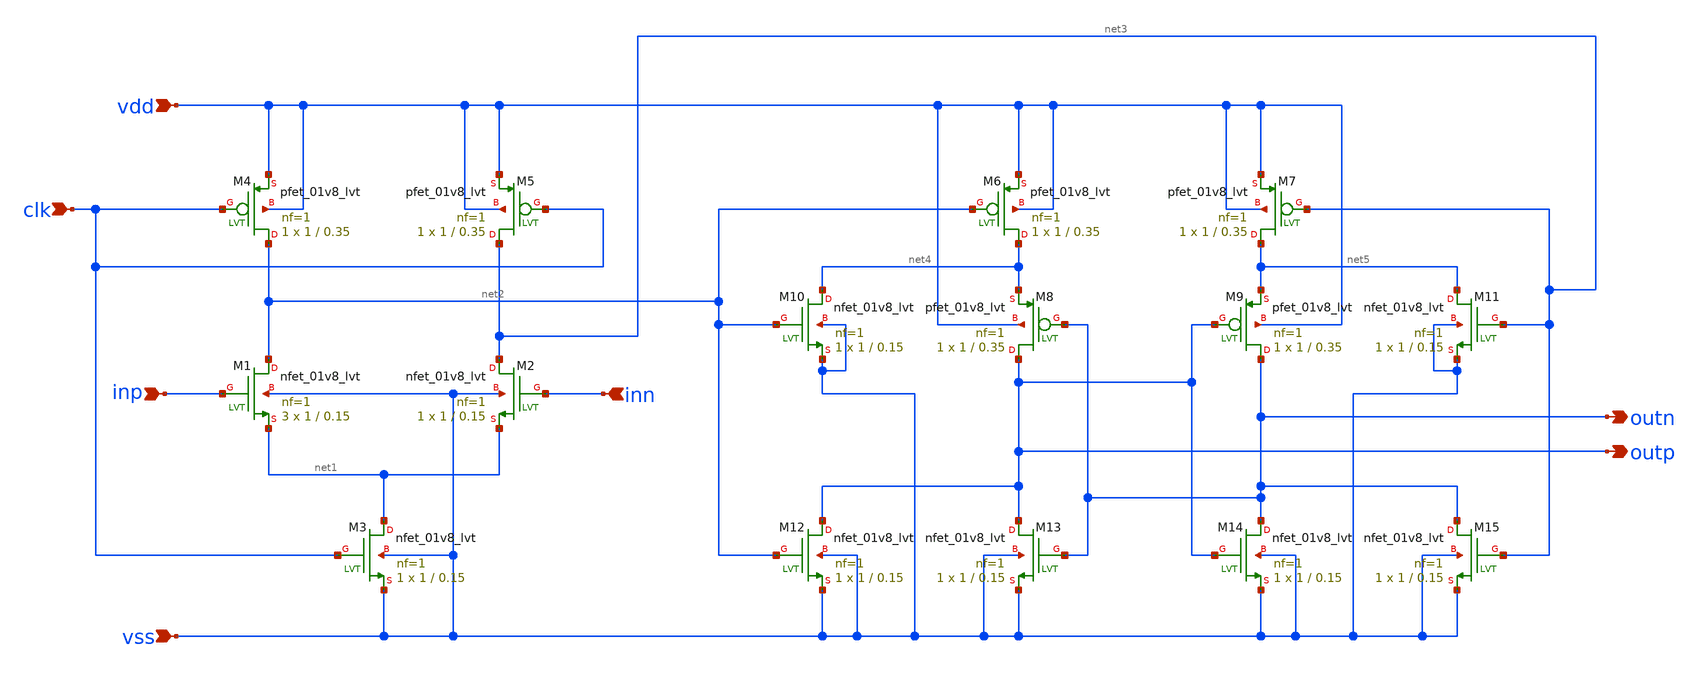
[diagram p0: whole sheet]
** sch_path: xschem/my_dynamic_comparator2.sch
**.subckt my_dynamic_comparator2 clk inn inp vdd vss outn outp
*.ipin clk
*.ipin inn
*.ipin inp
*.ipin vdd
*.ipin vss
*.opin outn
*.opin outp
XM1 net2 inp net1 vss sky130_fd_pr__nfet_01v8_lvt L=0.15 W=1 nf=1 ad='int((nf+1)/2) * W/nf * 0.29' as='int((nf+2)/2) * W/nf * 0.29'
+ pd='2*int((nf+1)/2) * (W/nf + 0.29)' ps='2*int((nf+2)/2) * (W/nf + 0.29)' nrd='0.29 / W' nrs='0.29 / W'
+ sa=0 sb=0 sd=0 mult=3 m=3
XM2 net3 inn net1 vss sky130_fd_pr__nfet_01v8_lvt L=0.15 W=1 nf=1 ad='int((nf+1)/2) * W/nf * 0.29' as='int((nf+2)/2) * W/nf * 0.29'
+ pd='2*int((nf+1)/2) * (W/nf + 0.29)' ps='2*int((nf+2)/2) * (W/nf + 0.29)' nrd='0.29 / W' nrs='0.29 / W'
+ sa=0 sb=0 sd=0 mult=1 m=1
XM3 net1 clk vss vss sky130_fd_pr__nfet_01v8_lvt L=0.15 W=1 nf=1 ad='int((nf+1)/2) * W/nf * 0.29' as='int((nf+2)/2) * W/nf * 0.29'
+ pd='2*int((nf+1)/2) * (W/nf + 0.29)' ps='2*int((nf+2)/2) * (W/nf + 0.29)' nrd='0.29 / W' nrs='0.29 / W'
+ sa=0 sb=0 sd=0 mult=1 m=1
XM4 net2 clk vdd vdd sky130_fd_pr__pfet_01v8_lvt L=0.35 W=1 nf=1 ad='int((nf+1)/2) * W/nf * 0.29' as='int((nf+2)/2) * W/nf * 0.29'
+ pd='2*int((nf+1)/2) * (W/nf + 0.29)' ps='2*int((nf+2)/2) * (W/nf + 0.29)' nrd='0.29 / W' nrs='0.29 / W'
+ sa=0 sb=0 sd=0 mult=1 m=1
XM5 net3 clk vdd vdd sky130_fd_pr__pfet_01v8_lvt L=0.35 W=1 nf=1 ad='int((nf+1)/2) * W/nf * 0.29' as='int((nf+2)/2) * W/nf * 0.29'
+ pd='2*int((nf+1)/2) * (W/nf + 0.29)' ps='2*int((nf+2)/2) * (W/nf + 0.29)' nrd='0.29 / W' nrs='0.29 / W'
+ sa=0 sb=0 sd=0 mult=1 m=1
XM6 net4 net2 vdd vdd sky130_fd_pr__pfet_01v8_lvt L=0.35 W=1 nf=1 ad='int((nf+1)/2) * W/nf * 0.29' as='int((nf+2)/2) * W/nf * 0.29'
+ pd='2*int((nf+1)/2) * (W/nf + 0.29)' ps='2*int((nf+2)/2) * (W/nf + 0.29)' nrd='0.29 / W' nrs='0.29 / W'
+ sa=0 sb=0 sd=0 mult=1 m=1
XM7 net5 net3 vdd vdd sky130_fd_pr__pfet_01v8_lvt L=0.35 W=1 nf=1 ad='int((nf+1)/2) * W/nf * 0.29' as='int((nf+2)/2) * W/nf * 0.29'
+ pd='2*int((nf+1)/2) * (W/nf + 0.29)' ps='2*int((nf+2)/2) * (W/nf + 0.29)' nrd='0.29 / W' nrs='0.29 / W'
+ sa=0 sb=0 sd=0 mult=1 m=1
XM8 outp outn net4 vdd sky130_fd_pr__pfet_01v8_lvt L=0.35 W=1 nf=1 ad='int((nf+1)/2) * W/nf * 0.29' as='int((nf+2)/2) * W/nf * 0.29'
+ pd='2*int((nf+1)/2) * (W/nf + 0.29)' ps='2*int((nf+2)/2) * (W/nf + 0.29)' nrd='0.29 / W' nrs='0.29 / W'
+ sa=0 sb=0 sd=0 mult=1 m=1
XM9 outn outp net5 vdd sky130_fd_pr__pfet_01v8_lvt L=0.35 W=1 nf=1 ad='int((nf+1)/2) * W/nf * 0.29' as='int((nf+2)/2) * W/nf * 0.29'
+ pd='2*int((nf+1)/2) * (W/nf + 0.29)' ps='2*int((nf+2)/2) * (W/nf + 0.29)' nrd='0.29 / W' nrs='0.29 / W'
+ sa=0 sb=0 sd=0 mult=1 m=1
XM10 net4 net2 vss vss sky130_fd_pr__nfet_01v8_lvt L=0.15 W=1 nf=1 ad='int((nf+1)/2) * W/nf * 0.29' as='int((nf+2)/2) * W/nf * 0.29'
+ pd='2*int((nf+1)/2) * (W/nf + 0.29)' ps='2*int((nf+2)/2) * (W/nf + 0.29)' nrd='0.29 / W' nrs='0.29 / W'
+ sa=0 sb=0 sd=0 mult=1 m=1
XM11 net5 net3 vss vss sky130_fd_pr__nfet_01v8_lvt L=0.15 W=1 nf=1 ad='int((nf+1)/2) * W/nf * 0.29' as='int((nf+2)/2) * W/nf * 0.29'
+ pd='2*int((nf+1)/2) * (W/nf + 0.29)' ps='2*int((nf+2)/2) * (W/nf + 0.29)' nrd='0.29 / W' nrs='0.29 / W'
+ sa=0 sb=0 sd=0 mult=1 m=1
XM12 outp net2 vss vss sky130_fd_pr__nfet_01v8_lvt L=0.15 W=1 nf=1 ad='int((nf+1)/2) * W/nf * 0.29' as='int((nf+2)/2) * W/nf * 0.29'
+ pd='2*int((nf+1)/2) * (W/nf + 0.29)' ps='2*int((nf+2)/2) * (W/nf + 0.29)' nrd='0.29 / W' nrs='0.29 / W'
+ sa=0 sb=0 sd=0 mult=1 m=1
XM13 outp outn vss vss sky130_fd_pr__nfet_01v8_lvt L=0.15 W=1 nf=1 ad='int((nf+1)/2) * W/nf * 0.29' as='int((nf+2)/2) * W/nf * 0.29'
+ pd='2*int((nf+1)/2) * (W/nf + 0.29)' ps='2*int((nf+2)/2) * (W/nf + 0.29)' nrd='0.29 / W' nrs='0.29 / W'
+ sa=0 sb=0 sd=0 mult=1 m=1
XM14 outn outp vss vss sky130_fd_pr__nfet_01v8_lvt L=0.15 W=1 nf=1 ad='int((nf+1)/2) * W/nf * 0.29' as='int((nf+2)/2) * W/nf * 0.29'
+ pd='2*int((nf+1)/2) * (W/nf + 0.29)' ps='2*int((nf+2)/2) * (W/nf + 0.29)' nrd='0.29 / W' nrs='0.29 / W'
+ sa=0 sb=0 sd=0 mult=1 m=1
XM15 outn net3 vss vss sky130_fd_pr__nfet_01v8_lvt L=0.15 W=1 nf=1 ad='int((nf+1)/2) * W/nf * 0.29' as='int((nf+2)/2) * W/nf * 0.29'
+ pd='2*int((nf+1)/2) * (W/nf + 0.29)' ps='2*int((nf+2)/2) * (W/nf + 0.29)' nrd='0.29 / W' nrs='0.29 / W'
+ sa=0 sb=0 sd=0 mult=1 m=1
**.ends
.end
